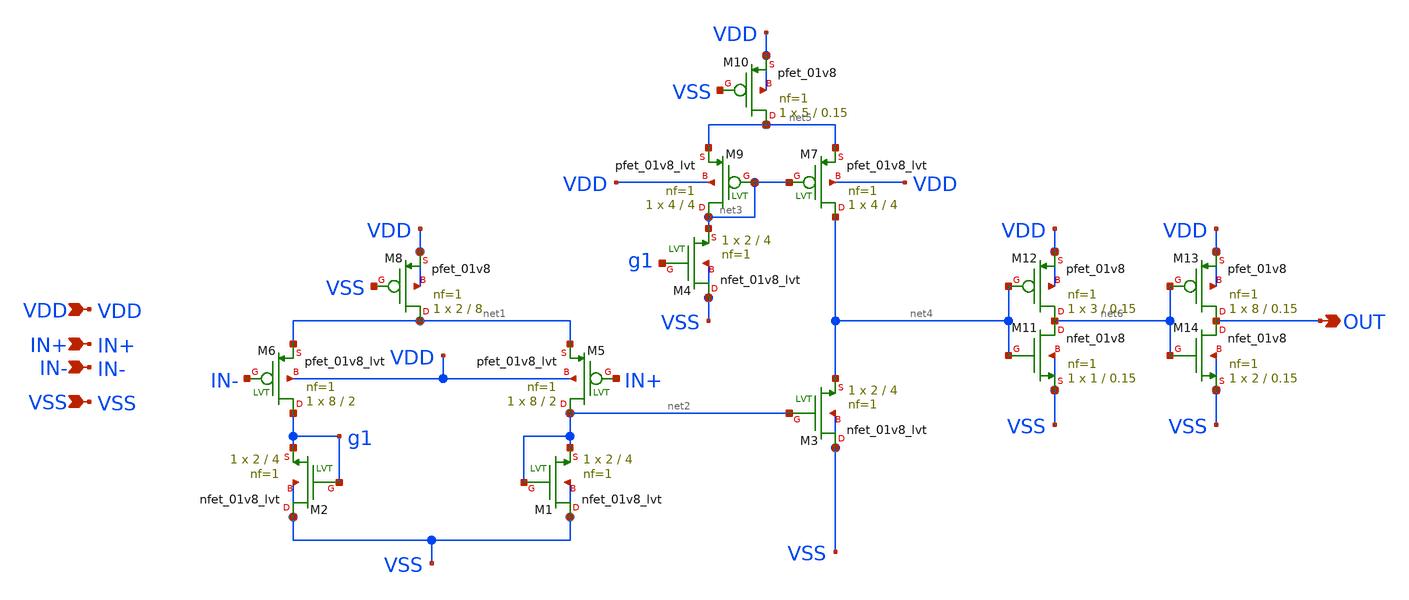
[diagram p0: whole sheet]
** sch_path: xschem/compr.sch
**.subckt compr IN+ OUT IN- VDD VSS
*.ipin IN+
*.opin OUT
*.ipin IN-
*.ipin VDD
*.ipin VSS
XM1 VSS net2 net2 VSS sky130_fd_pr__nfet_01v8_lvt L=4 W=2 nf=1 ad='int((nf+1)/2) * W/nf * 0.29' as='int((nf+2)/2) * W/nf * 0.29'
+ pd='2*int((nf+1)/2) * (W/nf + 0.29)' ps='2*int((nf+2)/2) * (W/nf + 0.29)' nrd='0.29 / W' nrs='0.29 / W'
+ sa=0 sb=0 sd=0 mult=1 m=1
XM2 VSS g1 g1 VSS sky130_fd_pr__nfet_01v8_lvt L=4 W=2 nf=1 ad='int((nf+1)/2) * W/nf * 0.29' as='int((nf+2)/2) * W/nf * 0.29'
+ pd='2*int((nf+1)/2) * (W/nf + 0.29)' ps='2*int((nf+2)/2) * (W/nf + 0.29)' nrd='0.29 / W' nrs='0.29 / W'
+ sa=0 sb=0 sd=0 mult=1 m=1
XM3 VSS net2 net4 VSS sky130_fd_pr__nfet_01v8_lvt L=4 W=2 nf=1 ad='int((nf+1)/2) * W/nf * 0.29' as='int((nf+2)/2) * W/nf * 0.29'
+ pd='2*int((nf+1)/2) * (W/nf + 0.29)' ps='2*int((nf+2)/2) * (W/nf + 0.29)' nrd='0.29 / W' nrs='0.29 / W'
+ sa=0 sb=0 sd=0 mult=1 m=1
XM4 VSS g1 net3 VSS sky130_fd_pr__nfet_01v8_lvt L=4 W=2 nf=1 ad='int((nf+1)/2) * W/nf * 0.29' as='int((nf+2)/2) * W/nf * 0.29'
+ pd='2*int((nf+1)/2) * (W/nf + 0.29)' ps='2*int((nf+2)/2) * (W/nf + 0.29)' nrd='0.29 / W' nrs='0.29 / W'
+ sa=0 sb=0 sd=0 mult=1 m=1
XM5 net2 IN+ net1 VDD sky130_fd_pr__pfet_01v8_lvt L=2 W=8 nf=1 ad='int((nf+1)/2) * W/nf * 0.29' as='int((nf+2)/2) * W/nf * 0.29'
+ pd='2*int((nf+1)/2) * (W/nf + 0.29)' ps='2*int((nf+2)/2) * (W/nf + 0.29)' nrd='0.29 / W' nrs='0.29 / W'
+ sa=0 sb=0 sd=0 mult=1 m=1
XM6 g1 IN- net1 VDD sky130_fd_pr__pfet_01v8_lvt L=2 W=8 nf=1 ad='int((nf+1)/2) * W/nf * 0.29' as='int((nf+2)/2) * W/nf * 0.29'
+ pd='2*int((nf+1)/2) * (W/nf + 0.29)' ps='2*int((nf+2)/2) * (W/nf + 0.29)' nrd='0.29 / W' nrs='0.29 / W'
+ sa=0 sb=0 sd=0 mult=1 m=1
XM7 net4 net3 net5 VDD sky130_fd_pr__pfet_01v8_lvt L=4 W=4 nf=1 ad='int((nf+1)/2) * W/nf * 0.29' as='int((nf+2)/2) * W/nf * 0.29'
+ pd='2*int((nf+1)/2) * (W/nf + 0.29)' ps='2*int((nf+2)/2) * (W/nf + 0.29)' nrd='0.29 / W' nrs='0.29 / W'
+ sa=0 sb=0 sd=0 mult=1 m=1
XM9 net3 net3 net5 VDD sky130_fd_pr__pfet_01v8_lvt L=4 W=4 nf=1 ad='int((nf+1)/2) * W/nf * 0.29' as='int((nf+2)/2) * W/nf * 0.29'
+ pd='2*int((nf+1)/2) * (W/nf + 0.29)' ps='2*int((nf+2)/2) * (W/nf + 0.29)' nrd='0.29 / W' nrs='0.29 / W'
+ sa=0 sb=0 sd=0 mult=1 m=1
XM8 net1 VSS VDD VDD sky130_fd_pr__pfet_01v8 L=8 W=2 nf=1 ad='int((nf+1)/2) * W/nf * 0.29' as='int((nf+2)/2) * W/nf * 0.29'
+ pd='2*int((nf+1)/2) * (W/nf + 0.29)' ps='2*int((nf+2)/2) * (W/nf + 0.29)' nrd='0.29 / W' nrs='0.29 / W'
+ sa=0 sb=0 sd=0 mult=1 m=1
XM10 net5 VSS VDD VDD sky130_fd_pr__pfet_01v8 L=0.15 W=5 nf=1 ad='int((nf+1)/2) * W/nf * 0.29' as='int((nf+2)/2) * W/nf * 0.29'
+ pd='2*int((nf+1)/2) * (W/nf + 0.29)' ps='2*int((nf+2)/2) * (W/nf + 0.29)' nrd='0.29 / W' nrs='0.29 / W'
+ sa=0 sb=0 sd=0 mult=1 m=1
XM14 OUT net6 VSS VSS sky130_fd_pr__nfet_01v8 L=0.15 W=2 nf=1 ad='int((nf+1)/2) * W/nf * 0.29' as='int((nf+2)/2) * W/nf * 0.29'
+ pd='2*int((nf+1)/2) * (W/nf + 0.29)' ps='2*int((nf+2)/2) * (W/nf + 0.29)' nrd='0.29 / W' nrs='0.29 / W'
+ sa=0 sb=0 sd=0 mult=1 m=1
XM13 OUT net6 VDD VDD sky130_fd_pr__pfet_01v8 L=0.15 W=8 nf=1 ad='int((nf+1)/2) * W/nf * 0.29' as='int((nf+2)/2) * W/nf * 0.29'
+ pd='2*int((nf+1)/2) * (W/nf + 0.29)' ps='2*int((nf+2)/2) * (W/nf + 0.29)' nrd='0.29 / W' nrs='0.29 / W'
+ sa=0 sb=0 sd=0 mult=1 m=1
XM11 net6 net4 VSS VSS sky130_fd_pr__nfet_01v8 L=0.15 W=1 nf=1 ad='int((nf+1)/2) * W/nf * 0.29' as='int((nf+2)/2) * W/nf * 0.29'
+ pd='2*int((nf+1)/2) * (W/nf + 0.29)' ps='2*int((nf+2)/2) * (W/nf + 0.29)' nrd='0.29 / W' nrs='0.29 / W'
+ sa=0 sb=0 sd=0 mult=1 m=1
XM12 net6 net4 VDD VDD sky130_fd_pr__pfet_01v8 L=0.15 W=3 nf=1 ad='int((nf+1)/2) * W/nf * 0.29' as='int((nf+2)/2) * W/nf * 0.29'
+ pd='2*int((nf+1)/2) * (W/nf + 0.29)' ps='2*int((nf+2)/2) * (W/nf + 0.29)' nrd='0.29 / W' nrs='0.29 / W'
+ sa=0 sb=0 sd=0 mult=1 m=1
**.ends
.end
